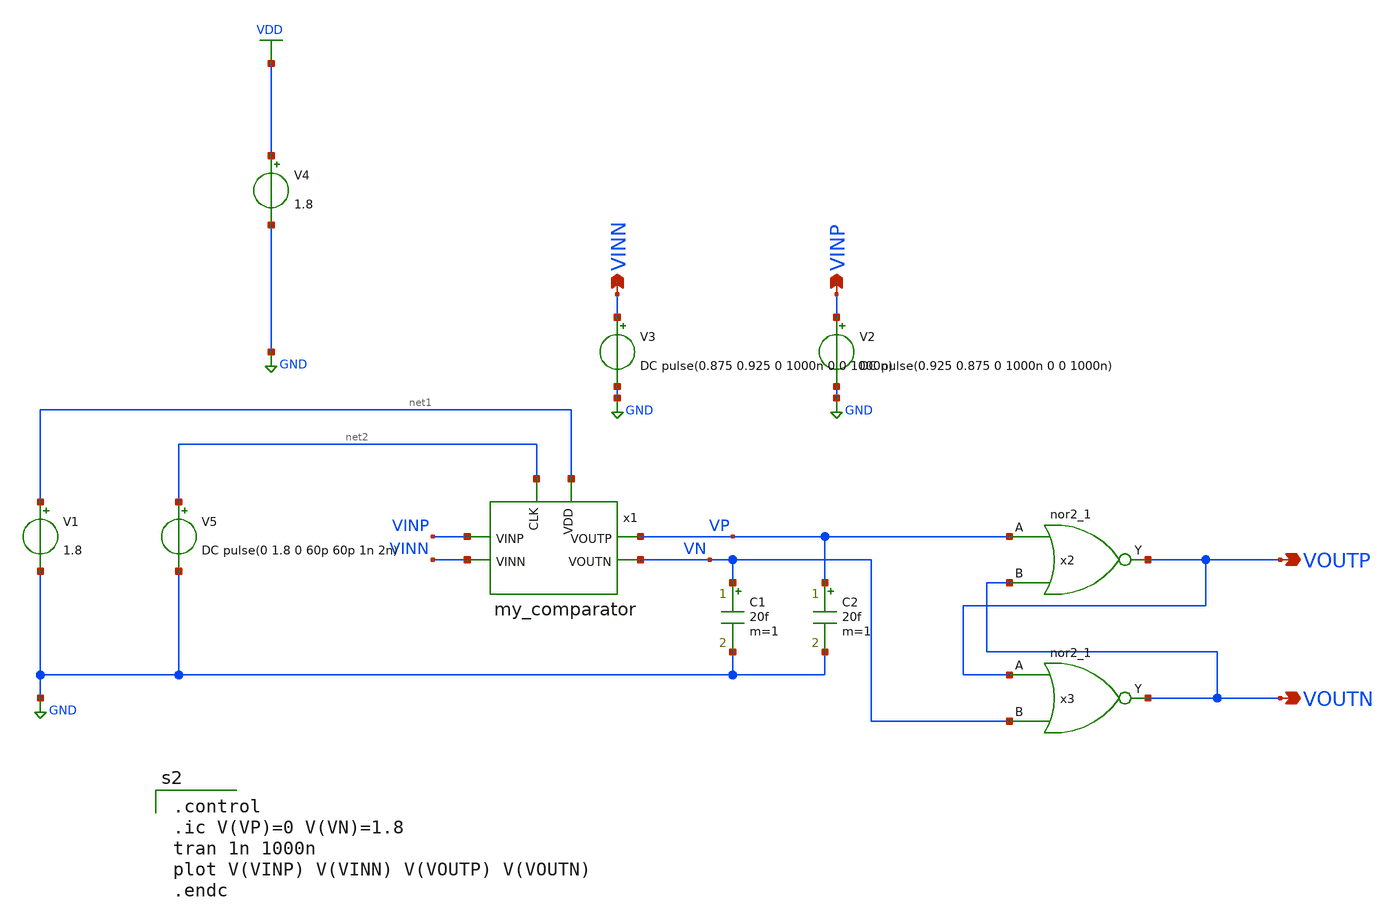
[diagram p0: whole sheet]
** sch_path: xschem/tb_my_comparator.sch
**.subckt tb_my_comparator VINP VINN VOUTP VOUTN
*.opin VINP
*.opin VINN
*.opin VOUTP
*.opin VOUTN
x1 net2 VP VN VINP VINN net1 my_comparator
V2 VINP GND DC pulse(0.925 0.875 0 1000n 0 0 1000n)
V3 VINN GND DC pulse(0.875 0.925 0 1000n 0 0 1000n)
V5 net2 GND DC pulse(0 1.8 0 60p 60p 1n 2n)
C1 VN GND 20f m=1
C2 VP GND 20f m=1
V1 net1 GND 1.8
x2 VP VOUTN GND GND VDD VDD VOUTP sky130_fd_sc_hd__nor2_1
x3 VOUTP VN GND GND VDD VDD VOUTN sky130_fd_sc_hd__nor2_1
V4 VDD GND 1.8
**** begin user architecture code
.lib $::SKYWATER_MODELS/sky130.lib.spice tt
.include $::PDKPATH/libs.ref/sky130_fd_sc_hvl/spice/sky130_fd_sc_hvl.spice
.include $::PDKPATH/libs.ref/sky130_fd_sc_hd/spice/sky130_fd_sc_hd.spice

.control
.ic V(VP)=0 V(VN)=1.8
tran 1n 1000n
plot V(VINP) V(VINN) V(VOUTP) V(VOUTN)
.endc

**** end user architecture code
**.ends

* expanding   symbol:  my_comparator.sym # of pins=6
** sym_path: xschem/my_comparator.sym
** sch_path: xschem/my_comparator.sch
.subckt my_comparator CLK VOUTP VOUTN VINP VINN VDD
*.ipin VDD
*.opin VOUTN
*.opin VOUTP
*.ipin CLK
*.ipin VINP
*.ipin VINN
XM2 net1 VINP net3 GND sky130_fd_pr__nfet_01v8_lvt L=0.15 W=1 nf=1 ad='int((nf+1)/2) * W/nf * 0.29' as='int((nf+2)/2) * W/nf * 0.29'
+ pd='2*int((nf+1)/2) * (W/nf + 0.29)' ps='2*int((nf+2)/2) * (W/nf + 0.29)' nrd='0.29 / W' nrs='0.29 / W'
+ sa=0 sb=0 sd=0 mult=MN m=MN
XM4 net1 CLK VDD VDD sky130_fd_pr__pfet_01v8_lvt L=0.35 W=1 nf=1 ad='int((nf+1)/2) * W/nf * 0.29' as='int((nf+2)/2) * W/nf * 0.29'
+ pd='2*int((nf+1)/2) * (W/nf + 0.29)' ps='2*int((nf+2)/2) * (W/nf + 0.29)' nrd='0.29 / W' nrs='0.29 / W'
+ sa=0 sb=0 sd=0 mult=MP m=MP
**** begin user architecture code


.param MP=1
.param MN=1


**** end user architecture code
XM5 net2 CLK VDD VDD sky130_fd_pr__pfet_01v8_lvt L=0.35 W=1 nf=1 ad='int((nf+1)/2) * W/nf * 0.29' as='int((nf+2)/2) * W/nf * 0.29'
+ pd='2*int((nf+1)/2) * (W/nf + 0.29)' ps='2*int((nf+2)/2) * (W/nf + 0.29)' nrd='0.29 / W' nrs='0.29 / W'
+ sa=0 sb=0 sd=0 mult=MP m=MP
XM6 net5 net2 VDD VDD sky130_fd_pr__pfet_01v8_lvt L=0.35 W=1 nf=1 ad='int((nf+1)/2) * W/nf * 0.29' as='int((nf+2)/2) * W/nf * 0.29'
+ pd='2*int((nf+1)/2) * (W/nf + 0.29)' ps='2*int((nf+2)/2) * (W/nf + 0.29)' nrd='0.29 / W' nrs='0.29 / W'
+ sa=0 sb=0 sd=0 mult=MP m=MP
XM7 net4 net1 VDD VDD sky130_fd_pr__pfet_01v8_lvt L=0.35 W=1 nf=1 ad='int((nf+1)/2) * W/nf * 0.29' as='int((nf+2)/2) * W/nf * 0.29'
+ pd='2*int((nf+1)/2) * (W/nf + 0.29)' ps='2*int((nf+2)/2) * (W/nf + 0.29)' nrd='0.29 / W' nrs='0.29 / W'
+ sa=0 sb=0 sd=0 mult=MP m=MP
XM8 VOUTP VOUTN net4 VDD sky130_fd_pr__pfet_01v8_lvt L=0.35 W=1 nf=1 ad='int((nf+1)/2) * W/nf * 0.29'
+ as='int((nf+2)/2) * W/nf * 0.29' pd='2*int((nf+1)/2) * (W/nf + 0.29)' ps='2*int((nf+2)/2) * (W/nf + 0.29)'
+ nrd='0.29 / W' nrs='0.29 / W' sa=0 sb=0 sd=0 mult=MP m=MP
XM9 VOUTN VOUTP net5 VDD sky130_fd_pr__pfet_01v8_lvt L=0.35 W=1 nf=1 ad='int((nf+1)/2) * W/nf * 0.29'
+ as='int((nf+2)/2) * W/nf * 0.29' pd='2*int((nf+1)/2) * (W/nf + 0.29)' ps='2*int((nf+2)/2) * (W/nf + 0.29)'
+ nrd='0.29 / W' nrs='0.29 / W' sa=0 sb=0 sd=0 mult=MP m=MP
XM1 net2 VINN net3 GND sky130_fd_pr__nfet_01v8_lvt L=0.15 W=1 nf=1 ad='int((nf+1)/2) * W/nf * 0.29' as='int((nf+2)/2) * W/nf * 0.29'
+ pd='2*int((nf+1)/2) * (W/nf + 0.29)' ps='2*int((nf+2)/2) * (W/nf + 0.29)' nrd='0.29 / W' nrs='0.29 / W'
+ sa=0 sb=0 sd=0 mult=MN m=MN
XM3 net3 CLK GND GND sky130_fd_pr__nfet_01v8_lvt L=0.15 W=1 nf=1 ad='int((nf+1)/2) * W/nf * 0.29' as='int((nf+2)/2) * W/nf * 0.29'
+ pd='2*int((nf+1)/2) * (W/nf + 0.29)' ps='2*int((nf+2)/2) * (W/nf + 0.29)' nrd='0.29 / W' nrs='0.29 / W'
+ sa=0 sb=0 sd=0 mult=MN m=MN
XM10 net5 net2 GND GND sky130_fd_pr__nfet_01v8_lvt L=0.15 W=1 nf=1 ad='int((nf+1)/2) * W/nf * 0.29' as='int((nf+2)/2) * W/nf * 0.29'
+ pd='2*int((nf+1)/2) * (W/nf + 0.29)' ps='2*int((nf+2)/2) * (W/nf + 0.29)' nrd='0.29 / W' nrs='0.29 / W'
+ sa=0 sb=0 sd=0 mult=MN m=MN
XM11 net4 net1 GND GND sky130_fd_pr__nfet_01v8_lvt L=0.15 W=1 nf=1 ad='int((nf+1)/2) * W/nf * 0.29' as='int((nf+2)/2) * W/nf * 0.29'
+ pd='2*int((nf+1)/2) * (W/nf + 0.29)' ps='2*int((nf+2)/2) * (W/nf + 0.29)' nrd='0.29 / W' nrs='0.29 / W'
+ sa=0 sb=0 sd=0 mult=MN m=MN
XM12 VOUTP net1 GND GND sky130_fd_pr__nfet_01v8_lvt L=0.15 W=1 nf=1 ad='int((nf+1)/2) * W/nf * 0.29'
+ as='int((nf+2)/2) * W/nf * 0.29' pd='2*int((nf+1)/2) * (W/nf + 0.29)' ps='2*int((nf+2)/2) * (W/nf + 0.29)'
+ nrd='0.29 / W' nrs='0.29 / W' sa=0 sb=0 sd=0 mult=MN m=MN
XM13 VOUTP VOUTN GND GND sky130_fd_pr__nfet_01v8_lvt L=0.15 W=1 nf=1 ad='int((nf+1)/2) * W/nf * 0.29'
+ as='int((nf+2)/2) * W/nf * 0.29' pd='2*int((nf+1)/2) * (W/nf + 0.29)' ps='2*int((nf+2)/2) * (W/nf + 0.29)'
+ nrd='0.29 / W' nrs='0.29 / W' sa=0 sb=0 sd=0 mult=MN m=MN
XM14 VOUTN net2 GND GND sky130_fd_pr__nfet_01v8_lvt L=0.15 W=1 nf=1 ad='int((nf+1)/2) * W/nf * 0.29'
+ as='int((nf+2)/2) * W/nf * 0.29' pd='2*int((nf+1)/2) * (W/nf + 0.29)' ps='2*int((nf+2)/2) * (W/nf + 0.29)'
+ nrd='0.29 / W' nrs='0.29 / W' sa=0 sb=0 sd=0 mult=MN m=MN
XM15 VOUTN VOUTP GND GND sky130_fd_pr__nfet_01v8_lvt L=0.15 W=1 nf=1 ad='int((nf+1)/2) * W/nf * 0.29'
+ as='int((nf+2)/2) * W/nf * 0.29' pd='2*int((nf+1)/2) * (W/nf + 0.29)' ps='2*int((nf+2)/2) * (W/nf + 0.29)'
+ nrd='0.29 / W' nrs='0.29 / W' sa=0 sb=0 sd=0 mult=MN m=MN
.ends

.GLOBAL GND
.GLOBAL VDD
.end
